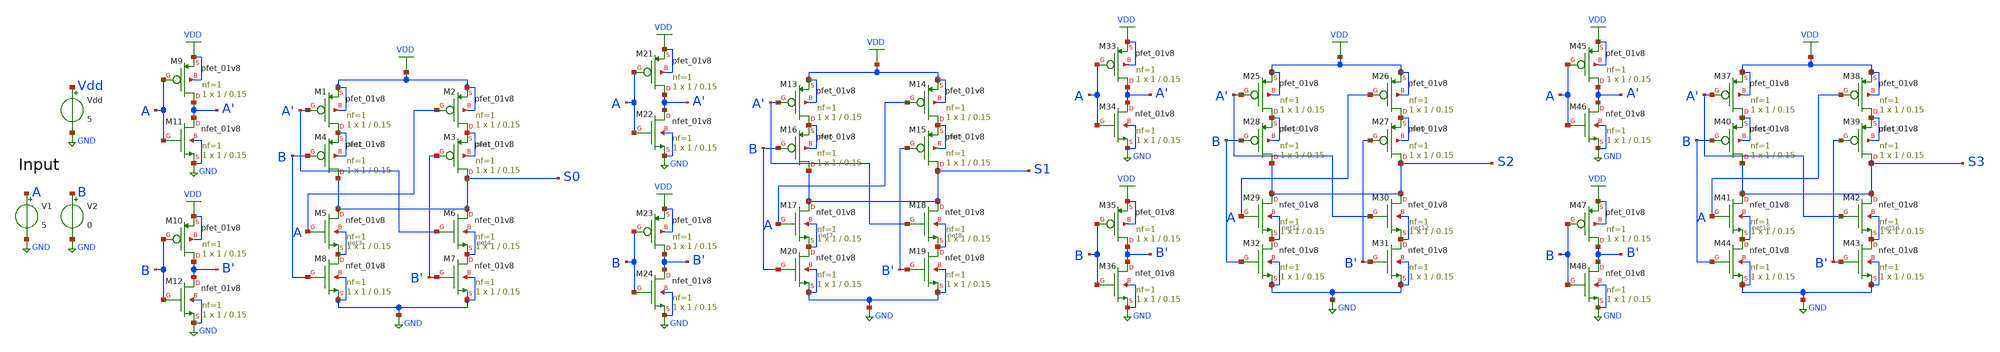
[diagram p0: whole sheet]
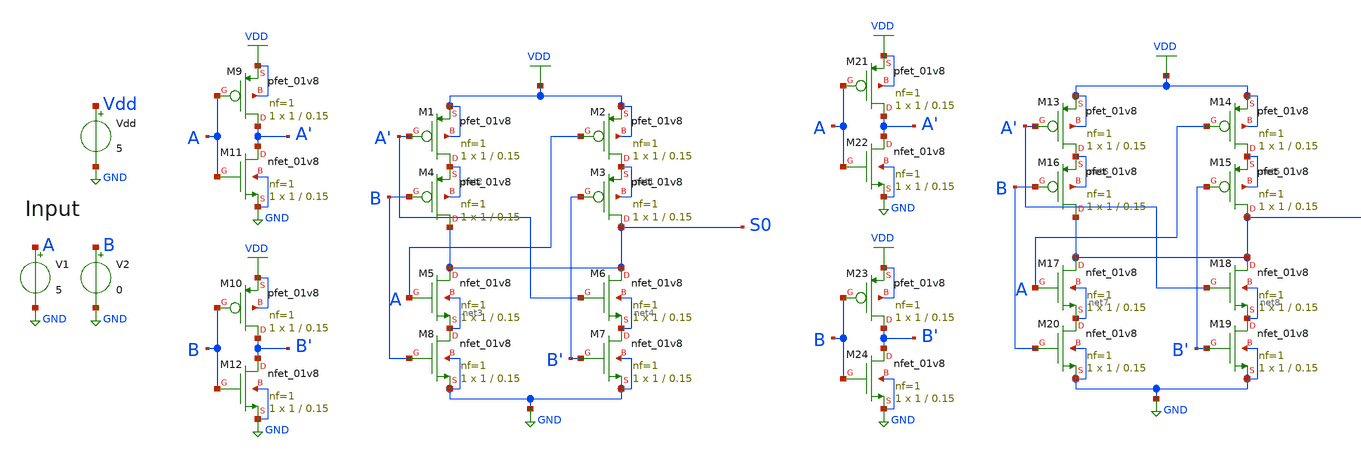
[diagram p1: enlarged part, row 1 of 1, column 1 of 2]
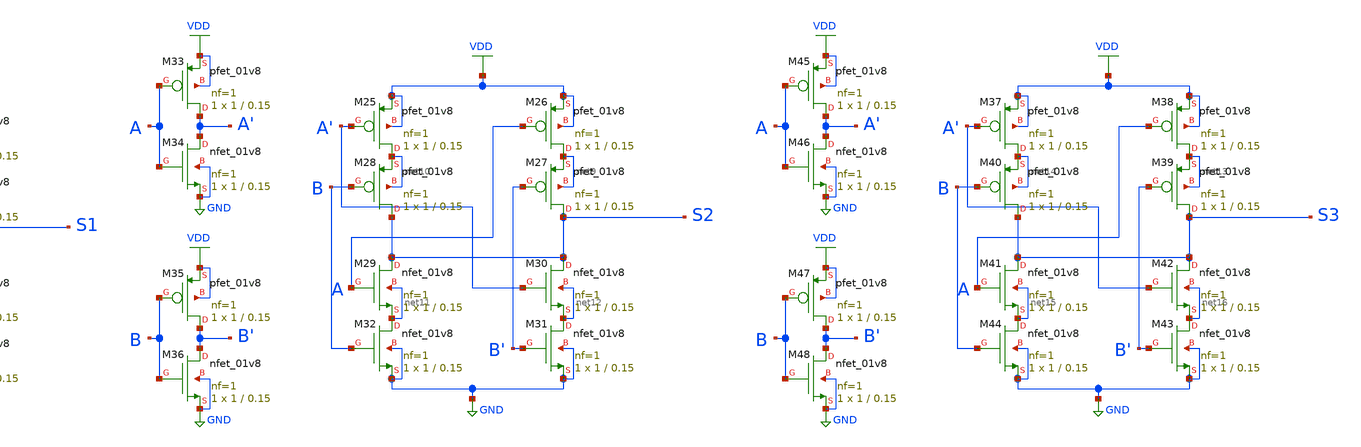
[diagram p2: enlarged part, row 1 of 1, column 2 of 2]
** sch_path: Bitwise_XOR.sch
**.subckt Bitwise_XOR
Vdd Vdd GND 5
V1 A GND 5
V2 B GND 0
XM1 net2 A' VDD VDD sky130_fd_pr__pfet_01v8 L=0.15 W=1 nf=1 ad='int((1 + 1)/2) * 1 / 1 * 0.29' as='int((1
+ + 2)/2) * 1 / 1 * 0.29' pd='2*int((1 + 1)/2) * (1 / 1 + 0.29)' ps='2*int((1 + 2)/2) * (1 / 1 + 0.29)' nrd='0.29
+ / 1 ' nrs='0.29 / 1 ' sa=0 sb=0 sd=0 mult=1 m=1
XM2 net1 A VDD VDD sky130_fd_pr__pfet_01v8 L=0.15 W=1 nf=1 ad='int((1 + 1)/2) * 1 / 1 * 0.29' as='int((1
+ + 2)/2) * 1 / 1 * 0.29' pd='2*int((1 + 1)/2) * (1 / 1 + 0.29)' ps='2*int((1 + 2)/2) * (1 / 1 + 0.29)' nrd='0.29
+ / 1 ' nrs='0.29 / 1 ' sa=0 sb=0 sd=0 mult=1 m=1
XM3 S0 B' net1 net1 sky130_fd_pr__pfet_01v8 L=0.15 W=1 nf=1 ad='int((1 + 1)/2) * 1 / 1 * 0.29' as='int((1 + 2)/2) * 1 / 1 * 0.29'
+ pd='2*int((1 + 1)/2) * (1 / 1 + 0.29)' ps='2*int((1 + 2)/2) * (1 / 1 + 0.29)' nrd='0.29 / 1 ' nrs='0.29 / 1 '
+ sa=0 sb=0 sd=0 mult=1 m=1
XM4 S0 B net2 net2 sky130_fd_pr__pfet_01v8 L=0.15 W=1 nf=1 ad='int((1 + 1)/2) * 1 / 1 * 0.29' as='int((1 + 2)/2) * 1 / 1 * 0.29'
+ pd='2*int((1 + 1)/2) * (1 / 1 + 0.29)' ps='2*int((1 + 2)/2) * (1 / 1 + 0.29)' nrd='0.29 / 1 ' nrs='0.29 / 1 '
+ sa=0 sb=0 sd=0 mult=1 m=1
XM5 S0 A net3 net3 sky130_fd_pr__nfet_01v8 L=0.15 W=1 nf=1 ad='int((1 + 1)/2) * 1 / 1 * 0.29' as='int((1 + 2)/2) * 1 / 1 * 0.29'
+ pd='2*int((1 + 1)/2) * (1 / 1 + 0.29)' ps='2*int((1 + 2)/2) * (1 / 1 + 0.29)' nrd='0.29 / 1 ' nrs='0.29 / 1 '
+ sa=0 sb=0 sd=0 mult=1 m=1
XM6 S0 A' net4 net4 sky130_fd_pr__nfet_01v8 L=0.15 W=1 nf=1 ad='int((1 + 1)/2) * 1 / 1 * 0.29' as='int((1
+ + 2)/2) * 1 / 1 * 0.29' pd='2*int((1 + 1)/2) * (1 / 1 + 0.29)' ps='2*int((1 + 2)/2) * (1 / 1 + 0.29)' nrd='0.29
+ / 1 ' nrs='0.29 / 1 ' sa=0 sb=0 sd=0 mult=1 m=1
XM7 net4 B' GND GND sky130_fd_pr__nfet_01v8 L=0.15 W=1 nf=1 ad='int((1 + 1)/2) * 1 / 1 * 0.29' as='int((1 + 2)/2) * 1 / 1 * 0.29'
+ pd='2*int((1 + 1)/2) * (1 / 1 + 0.29)' ps='2*int((1 + 2)/2) * (1 / 1 + 0.29)' nrd='0.29 / 1 ' nrs='0.29 / 1 '
+ sa=0 sb=0 sd=0 mult=1 m=1
XM8 net3 B GND GND sky130_fd_pr__nfet_01v8 L=0.15 W=1 nf=1 ad='int((1 + 1)/2) * 1 / 1 * 0.29' as='int((1 + 2)/2) * 1 / 1 * 0.29'
+ pd='2*int((1 + 1)/2) * (1 / 1 + 0.29)' ps='2*int((1 + 2)/2) * (1 / 1 + 0.29)' nrd='0.29 / 1 ' nrs='0.29 / 1 '
+ sa=0 sb=0 sd=0 mult=1 m=1
XM9 A' A VDD VDD sky130_fd_pr__pfet_01v8 L=0.15 W=1 nf=1 ad='int((1 + 1)/2) * 1 / 1 * 0.29' as='int((1
+ + 2)/2) * 1 / 1 * 0.29' pd='2*int((1 + 1)/2) * (1 / 1 + 0.29)' ps='2*int((1 + 2)/2) * (1 / 1 + 0.29)' nrd='0.29
+ / 1 ' nrs='0.29 / 1 ' sa=0 sb=0 sd=0 mult=1 m=1
XM11 A' A GND GND sky130_fd_pr__nfet_01v8 L=0.15 W=1 nf=1 ad='int((1 + 1)/2) * 1 / 1 * 0.29' as='int((1 + 2)/2) * 1 / 1 * 0.29'
+ pd='2*int((1 + 1)/2) * (1 / 1 + 0.29)' ps='2*int((1 + 2)/2) * (1 / 1 + 0.29)' nrd='0.29 / 1 ' nrs='0.29 / 1 '
+ sa=0 sb=0 sd=0 mult=1 m=1
XM10 B' B VDD VDD sky130_fd_pr__pfet_01v8 L=0.15 W=1 nf=1 ad='int((1 + 1)/2) * 1 / 1 * 0.29' as='int((1
+ + 2)/2) * 1 / 1 * 0.29' pd='2*int((1 + 1)/2) * (1 / 1 + 0.29)' ps='2*int((1 + 2)/2) * (1 / 1 + 0.29)' nrd='0.29
+ / 1 ' nrs='0.29 / 1 ' sa=0 sb=0 sd=0 mult=1 m=1
XM12 B' B GND GND sky130_fd_pr__nfet_01v8 L=0.15 W=1 nf=1 ad='int((1 + 1)/2) * 1 / 1 * 0.29' as='int((1 + 2)/2) * 1 / 1 * 0.29'
+ pd='2*int((1 + 1)/2) * (1 / 1 + 0.29)' ps='2*int((1 + 2)/2) * (1 / 1 + 0.29)' nrd='0.29 / 1 ' nrs='0.29 / 1 '
+ sa=0 sb=0 sd=0 mult=1 m=1
XM13 net6 A' VDD VDD sky130_fd_pr__pfet_01v8 L=0.15 W=1 nf=1 ad='int((1 + 1)/2) * 1 / 1 * 0.29' as='int((1
+ + 2)/2) * 1 / 1 * 0.29' pd='2*int((1 + 1)/2) * (1 / 1 + 0.29)' ps='2*int((1 + 2)/2) * (1 / 1 + 0.29)' nrd='0.29
+ / 1 ' nrs='0.29 / 1 ' sa=0 sb=0 sd=0 mult=1 m=1
XM14 net5 A VDD VDD sky130_fd_pr__pfet_01v8 L=0.15 W=1 nf=1 ad='int((1 + 1)/2) * 1 / 1 * 0.29' as='int((1
+ + 2)/2) * 1 / 1 * 0.29' pd='2*int((1 + 1)/2) * (1 / 1 + 0.29)' ps='2*int((1 + 2)/2) * (1 / 1 + 0.29)' nrd='0.29
+ / 1 ' nrs='0.29 / 1 ' sa=0 sb=0 sd=0 mult=1 m=1
XM15 S1 B' net5 net5 sky130_fd_pr__pfet_01v8 L=0.15 W=1 nf=1 ad='int((1 + 1)/2) * 1 / 1 * 0.29' as='int((1 + 2)/2) * 1 / 1 * 0.29'
+ pd='2*int((1 + 1)/2) * (1 / 1 + 0.29)' ps='2*int((1 + 2)/2) * (1 / 1 + 0.29)' nrd='0.29 / 1 ' nrs='0.29 / 1 '
+ sa=0 sb=0 sd=0 mult=1 m=1
XM16 S1 B net6 net6 sky130_fd_pr__pfet_01v8 L=0.15 W=1 nf=1 ad='int((1 + 1)/2) * 1 / 1 * 0.29' as='int((1 + 2)/2) * 1 / 1 * 0.29'
+ pd='2*int((1 + 1)/2) * (1 / 1 + 0.29)' ps='2*int((1 + 2)/2) * (1 / 1 + 0.29)' nrd='0.29 / 1 ' nrs='0.29 / 1 '
+ sa=0 sb=0 sd=0 mult=1 m=1
XM17 S1 A net7 net7 sky130_fd_pr__nfet_01v8 L=0.15 W=1 nf=1 ad='int((1 + 1)/2) * 1 / 1 * 0.29' as='int((1 + 2)/2) * 1 / 1 * 0.29'
+ pd='2*int((1 + 1)/2) * (1 / 1 + 0.29)' ps='2*int((1 + 2)/2) * (1 / 1 + 0.29)' nrd='0.29 / 1 ' nrs='0.29 / 1 '
+ sa=0 sb=0 sd=0 mult=1 m=1
XM18 S1 A' net8 net8 sky130_fd_pr__nfet_01v8 L=0.15 W=1 nf=1 ad='int((1 + 1)/2) * 1 / 1 * 0.29' as='int((1
+ + 2)/2) * 1 / 1 * 0.29' pd='2*int((1 + 1)/2) * (1 / 1 + 0.29)' ps='2*int((1 + 2)/2) * (1 / 1 + 0.29)' nrd='0.29
+ / 1 ' nrs='0.29 / 1 ' sa=0 sb=0 sd=0 mult=1 m=1
XM19 net8 B' GND GND sky130_fd_pr__nfet_01v8 L=0.15 W=1 nf=1 ad='int((1 + 1)/2) * 1 / 1 * 0.29' as='int((1 + 2)/2) * 1 / 1 * 0.29'
+ pd='2*int((1 + 1)/2) * (1 / 1 + 0.29)' ps='2*int((1 + 2)/2) * (1 / 1 + 0.29)' nrd='0.29 / 1 ' nrs='0.29 / 1 '
+ sa=0 sb=0 sd=0 mult=1 m=1
XM20 net7 B GND GND sky130_fd_pr__nfet_01v8 L=0.15 W=1 nf=1 ad='int((1 + 1)/2) * 1 / 1 * 0.29' as='int((1 + 2)/2) * 1 / 1 * 0.29'
+ pd='2*int((1 + 1)/2) * (1 / 1 + 0.29)' ps='2*int((1 + 2)/2) * (1 / 1 + 0.29)' nrd='0.29 / 1 ' nrs='0.29 / 1 '
+ sa=0 sb=0 sd=0 mult=1 m=1
XM21 A' A VDD VDD sky130_fd_pr__pfet_01v8 L=0.15 W=1 nf=1 ad='int((1 + 1)/2) * 1 / 1 * 0.29' as='int((1
+ + 2)/2) * 1 / 1 * 0.29' pd='2*int((1 + 1)/2) * (1 / 1 + 0.29)' ps='2*int((1 + 2)/2) * (1 / 1 + 0.29)' nrd='0.29
+ / 1 ' nrs='0.29 / 1 ' sa=0 sb=0 sd=0 mult=1 m=1
XM22 A' A GND GND sky130_fd_pr__nfet_01v8 L=0.15 W=1 nf=1 ad='int((1 + 1)/2) * 1 / 1 * 0.29' as='int((1 + 2)/2) * 1 / 1 * 0.29'
+ pd='2*int((1 + 1)/2) * (1 / 1 + 0.29)' ps='2*int((1 + 2)/2) * (1 / 1 + 0.29)' nrd='0.29 / 1 ' nrs='0.29 / 1 '
+ sa=0 sb=0 sd=0 mult=1 m=1
XM23 B' B VDD VDD sky130_fd_pr__pfet_01v8 L=0.15 W=1 nf=1 ad='int((1 + 1)/2) * 1 / 1 * 0.29' as='int((1
+ + 2)/2) * 1 / 1 * 0.29' pd='2*int((1 + 1)/2) * (1 / 1 + 0.29)' ps='2*int((1 + 2)/2) * (1 / 1 + 0.29)' nrd='0.29
+ / 1 ' nrs='0.29 / 1 ' sa=0 sb=0 sd=0 mult=1 m=1
XM24 B' B GND GND sky130_fd_pr__nfet_01v8 L=0.15 W=1 nf=1 ad='int((1 + 1)/2) * 1 / 1 * 0.29' as='int((1 + 2)/2) * 1 / 1 * 0.29'
+ pd='2*int((1 + 1)/2) * (1 / 1 + 0.29)' ps='2*int((1 + 2)/2) * (1 / 1 + 0.29)' nrd='0.29 / 1 ' nrs='0.29 / 1 '
+ sa=0 sb=0 sd=0 mult=1 m=1
XM25 net10 A' VDD VDD sky130_fd_pr__pfet_01v8 L=0.15 W=1 nf=1 ad='int((1 + 1)/2) * 1 / 1 * 0.29' as='int((1
+ + 2)/2) * 1 / 1 * 0.29' pd='2*int((1 + 1)/2) * (1 / 1 + 0.29)' ps='2*int((1 + 2)/2) * (1 / 1 + 0.29)' nrd='0.29
+ / 1 ' nrs='0.29 / 1 ' sa=0 sb=0 sd=0 mult=1 m=1
XM26 net9 A VDD VDD sky130_fd_pr__pfet_01v8 L=0.15 W=1 nf=1 ad='int((1 + 1)/2) * 1 / 1 * 0.29' as='int((1
+ + 2)/2) * 1 / 1 * 0.29' pd='2*int((1 + 1)/2) * (1 / 1 + 0.29)' ps='2*int((1 + 2)/2) * (1 / 1 + 0.29)' nrd='0.29
+ / 1 ' nrs='0.29 / 1 ' sa=0 sb=0 sd=0 mult=1 m=1
XM27 S2 B' net9 net9 sky130_fd_pr__pfet_01v8 L=0.15 W=1 nf=1 ad='int((1 + 1)/2) * 1 / 1 * 0.29' as='int((1 + 2)/2) * 1 / 1 * 0.29'
+ pd='2*int((1 + 1)/2) * (1 / 1 + 0.29)' ps='2*int((1 + 2)/2) * (1 / 1 + 0.29)' nrd='0.29 / 1 ' nrs='0.29 / 1 '
+ sa=0 sb=0 sd=0 mult=1 m=1
XM28 S2 B net10 net10 sky130_fd_pr__pfet_01v8 L=0.15 W=1 nf=1 ad='int((1 + 1)/2) * 1 / 1 * 0.29' as='int((1 + 2)/2) * 1 / 1 * 0.29'
+ pd='2*int((1 + 1)/2) * (1 / 1 + 0.29)' ps='2*int((1 + 2)/2) * (1 / 1 + 0.29)' nrd='0.29 / 1 ' nrs='0.29 / 1 '
+ sa=0 sb=0 sd=0 mult=1 m=1
XM29 S2 A net11 net11 sky130_fd_pr__nfet_01v8 L=0.15 W=1 nf=1 ad='int((1 + 1)/2) * 1 / 1 * 0.29' as='int((1 + 2)/2) * 1 / 1 * 0.29'
+ pd='2*int((1 + 1)/2) * (1 / 1 + 0.29)' ps='2*int((1 + 2)/2) * (1 / 1 + 0.29)' nrd='0.29 / 1 ' nrs='0.29 / 1 '
+ sa=0 sb=0 sd=0 mult=1 m=1
XM30 S2 A' net12 net12 sky130_fd_pr__nfet_01v8 L=0.15 W=1 nf=1 ad='int((1 + 1)/2) * 1 / 1 * 0.29' as='int((1
+ + 2)/2) * 1 / 1 * 0.29' pd='2*int((1 + 1)/2) * (1 / 1 + 0.29)' ps='2*int((1 + 2)/2) * (1 / 1 + 0.29)' nrd='0.29
+ / 1 ' nrs='0.29 / 1 ' sa=0 sb=0 sd=0 mult=1 m=1
XM31 net12 B' GND GND sky130_fd_pr__nfet_01v8 L=0.15 W=1 nf=1 ad='int((1 + 1)/2) * 1 / 1 * 0.29' as='int((1 + 2)/2) * 1 / 1 * 0.29'
+ pd='2*int((1 + 1)/2) * (1 / 1 + 0.29)' ps='2*int((1 + 2)/2) * (1 / 1 + 0.29)' nrd='0.29 / 1 ' nrs='0.29 / 1 '
+ sa=0 sb=0 sd=0 mult=1 m=1
XM32 net11 B GND GND sky130_fd_pr__nfet_01v8 L=0.15 W=1 nf=1 ad='int((1 + 1)/2) * 1 / 1 * 0.29' as='int((1 + 2)/2) * 1 / 1 * 0.29'
+ pd='2*int((1 + 1)/2) * (1 / 1 + 0.29)' ps='2*int((1 + 2)/2) * (1 / 1 + 0.29)' nrd='0.29 / 1 ' nrs='0.29 / 1 '
+ sa=0 sb=0 sd=0 mult=1 m=1
XM33 A' A VDD VDD sky130_fd_pr__pfet_01v8 L=0.15 W=1 nf=1 ad='int((1 + 1)/2) * 1 / 1 * 0.29' as='int((1
+ + 2)/2) * 1 / 1 * 0.29' pd='2*int((1 + 1)/2) * (1 / 1 + 0.29)' ps='2*int((1 + 2)/2) * (1 / 1 + 0.29)' nrd='0.29
+ / 1 ' nrs='0.29 / 1 ' sa=0 sb=0 sd=0 mult=1 m=1
XM34 A' A GND GND sky130_fd_pr__nfet_01v8 L=0.15 W=1 nf=1 ad='int((1 + 1)/2) * 1 / 1 * 0.29' as='int((1 + 2)/2) * 1 / 1 * 0.29'
+ pd='2*int((1 + 1)/2) * (1 / 1 + 0.29)' ps='2*int((1 + 2)/2) * (1 / 1 + 0.29)' nrd='0.29 / 1 ' nrs='0.29 / 1 '
+ sa=0 sb=0 sd=0 mult=1 m=1
XM35 B' B VDD VDD sky130_fd_pr__pfet_01v8 L=0.15 W=1 nf=1 ad='int((1 + 1)/2) * 1 / 1 * 0.29' as='int((1
+ + 2)/2) * 1 / 1 * 0.29' pd='2*int((1 + 1)/2) * (1 / 1 + 0.29)' ps='2*int((1 + 2)/2) * (1 / 1 + 0.29)' nrd='0.29
+ / 1 ' nrs='0.29 / 1 ' sa=0 sb=0 sd=0 mult=1 m=1
XM36 B' B GND GND sky130_fd_pr__nfet_01v8 L=0.15 W=1 nf=1 ad='int((1 + 1)/2) * 1 / 1 * 0.29' as='int((1 + 2)/2) * 1 / 1 * 0.29'
+ pd='2*int((1 + 1)/2) * (1 / 1 + 0.29)' ps='2*int((1 + 2)/2) * (1 / 1 + 0.29)' nrd='0.29 / 1 ' nrs='0.29 / 1 '
+ sa=0 sb=0 sd=0 mult=1 m=1
XM37 net14 A' VDD VDD sky130_fd_pr__pfet_01v8 L=0.15 W=1 nf=1 ad='int((1 + 1)/2) * 1 / 1 * 0.29' as='int((1
+ + 2)/2) * 1 / 1 * 0.29' pd='2*int((1 + 1)/2) * (1 / 1 + 0.29)' ps='2*int((1 + 2)/2) * (1 / 1 + 0.29)' nrd='0.29
+ / 1 ' nrs='0.29 / 1 ' sa=0 sb=0 sd=0 mult=1 m=1
XM38 net13 A VDD VDD sky130_fd_pr__pfet_01v8 L=0.15 W=1 nf=1 ad='int((1 + 1)/2) * 1 / 1 * 0.29' as='int((1
+ + 2)/2) * 1 / 1 * 0.29' pd='2*int((1 + 1)/2) * (1 / 1 + 0.29)' ps='2*int((1 + 2)/2) * (1 / 1 + 0.29)' nrd='0.29
+ / 1 ' nrs='0.29 / 1 ' sa=0 sb=0 sd=0 mult=1 m=1
XM39 S3 B' net13 net13 sky130_fd_pr__pfet_01v8 L=0.15 W=1 nf=1 ad='int((1 + 1)/2) * 1 / 1 * 0.29' as='int((1 + 2)/2) * 1 / 1 * 0.29'
+ pd='2*int((1 + 1)/2) * (1 / 1 + 0.29)' ps='2*int((1 + 2)/2) * (1 / 1 + 0.29)' nrd='0.29 / 1 ' nrs='0.29 / 1 '
+ sa=0 sb=0 sd=0 mult=1 m=1
XM40 S3 B net14 net14 sky130_fd_pr__pfet_01v8 L=0.15 W=1 nf=1 ad='int((1 + 1)/2) * 1 / 1 * 0.29' as='int((1 + 2)/2) * 1 / 1 * 0.29'
+ pd='2*int((1 + 1)/2) * (1 / 1 + 0.29)' ps='2*int((1 + 2)/2) * (1 / 1 + 0.29)' nrd='0.29 / 1 ' nrs='0.29 / 1 '
+ sa=0 sb=0 sd=0 mult=1 m=1
XM41 S3 A net15 net15 sky130_fd_pr__nfet_01v8 L=0.15 W=1 nf=1 ad='int((1 + 1)/2) * 1 / 1 * 0.29' as='int((1 + 2)/2) * 1 / 1 * 0.29'
+ pd='2*int((1 + 1)/2) * (1 / 1 + 0.29)' ps='2*int((1 + 2)/2) * (1 / 1 + 0.29)' nrd='0.29 / 1 ' nrs='0.29 / 1 '
+ sa=0 sb=0 sd=0 mult=1 m=1
XM42 S3 A' net16 net16 sky130_fd_pr__nfet_01v8 L=0.15 W=1 nf=1 ad='int((1 + 1)/2) * 1 / 1 * 0.29' as='int((1
+ + 2)/2) * 1 / 1 * 0.29' pd='2*int((1 + 1)/2) * (1 / 1 + 0.29)' ps='2*int((1 + 2)/2) * (1 / 1 + 0.29)' nrd='0.29
+ / 1 ' nrs='0.29 / 1 ' sa=0 sb=0 sd=0 mult=1 m=1
XM43 net16 B' GND GND sky130_fd_pr__nfet_01v8 L=0.15 W=1 nf=1 ad='int((1 + 1)/2) * 1 / 1 * 0.29' as='int((1 + 2)/2) * 1 / 1 * 0.29'
+ pd='2*int((1 + 1)/2) * (1 / 1 + 0.29)' ps='2*int((1 + 2)/2) * (1 / 1 + 0.29)' nrd='0.29 / 1 ' nrs='0.29 / 1 '
+ sa=0 sb=0 sd=0 mult=1 m=1
XM44 net15 B GND GND sky130_fd_pr__nfet_01v8 L=0.15 W=1 nf=1 ad='int((1 + 1)/2) * 1 / 1 * 0.29' as='int((1 + 2)/2) * 1 / 1 * 0.29'
+ pd='2*int((1 + 1)/2) * (1 / 1 + 0.29)' ps='2*int((1 + 2)/2) * (1 / 1 + 0.29)' nrd='0.29 / 1 ' nrs='0.29 / 1 '
+ sa=0 sb=0 sd=0 mult=1 m=1
XM45 A' A VDD VDD sky130_fd_pr__pfet_01v8 L=0.15 W=1 nf=1 ad='int((1 + 1)/2) * 1 / 1 * 0.29' as='int((1
+ + 2)/2) * 1 / 1 * 0.29' pd='2*int((1 + 1)/2) * (1 / 1 + 0.29)' ps='2*int((1 + 2)/2) * (1 / 1 + 0.29)' nrd='0.29
+ / 1 ' nrs='0.29 / 1 ' sa=0 sb=0 sd=0 mult=1 m=1
XM46 A' A GND GND sky130_fd_pr__nfet_01v8 L=0.15 W=1 nf=1 ad='int((1 + 1)/2) * 1 / 1 * 0.29' as='int((1 + 2)/2) * 1 / 1 * 0.29'
+ pd='2*int((1 + 1)/2) * (1 / 1 + 0.29)' ps='2*int((1 + 2)/2) * (1 / 1 + 0.29)' nrd='0.29 / 1 ' nrs='0.29 / 1 '
+ sa=0 sb=0 sd=0 mult=1 m=1
XM47 B' B VDD VDD sky130_fd_pr__pfet_01v8 L=0.15 W=1 nf=1 ad='int((1 + 1)/2) * 1 / 1 * 0.29' as='int((1
+ + 2)/2) * 1 / 1 * 0.29' pd='2*int((1 + 1)/2) * (1 / 1 + 0.29)' ps='2*int((1 + 2)/2) * (1 / 1 + 0.29)' nrd='0.29
+ / 1 ' nrs='0.29 / 1 ' sa=0 sb=0 sd=0 mult=1 m=1
XM48 B' B GND GND sky130_fd_pr__nfet_01v8 L=0.15 W=1 nf=1 ad='int((1 + 1)/2) * 1 / 1 * 0.29' as='int((1 + 2)/2) * 1 / 1 * 0.29'
+ pd='2*int((1 + 1)/2) * (1 / 1 + 0.29)' ps='2*int((1 + 2)/2) * (1 / 1 + 0.29)' nrd='0.29 / 1 ' nrs='0.29 / 1 '
+ sa=0 sb=0 sd=0 mult=1 m=1
**** begin user architecture code

.lib /usr/local/share/pdk/sky130A/libs.tech/ngspice/sky130.lib.spice tt
.tran 1u 1
.save all
.end

**** end user architecture code
**.ends
.GLOBAL GND
.GLOBAL VDD
.end
